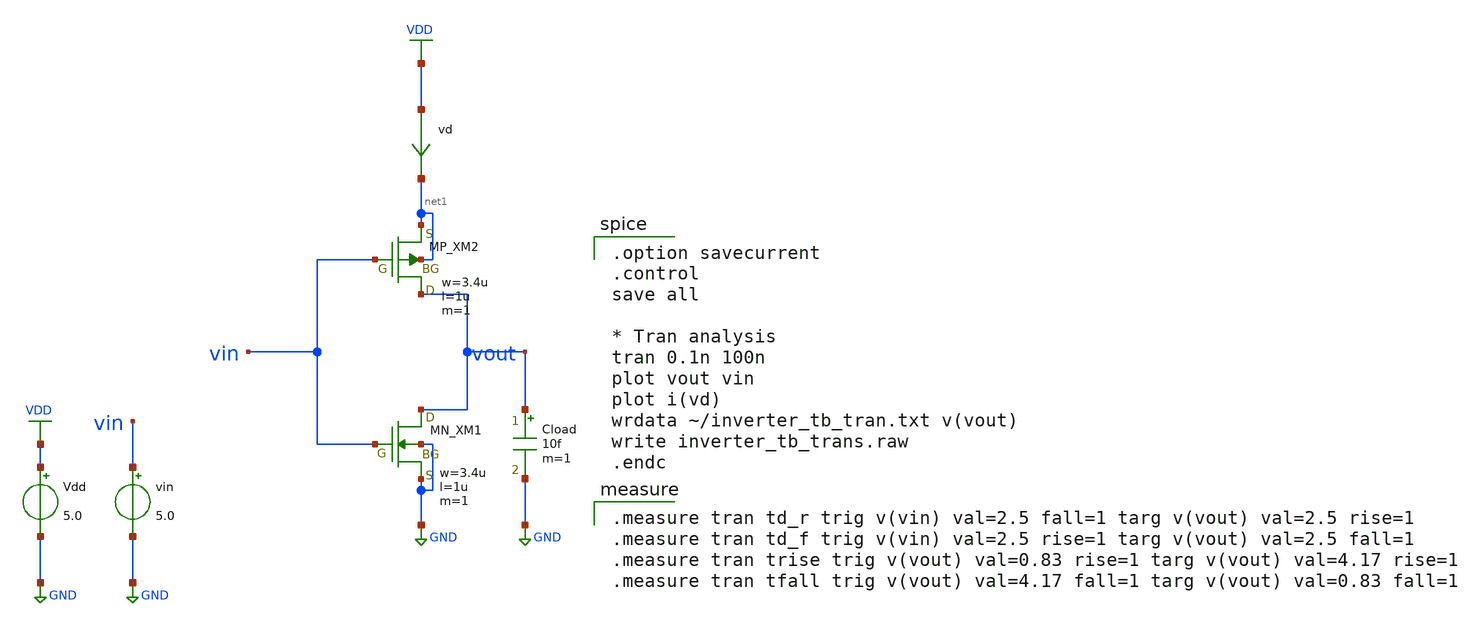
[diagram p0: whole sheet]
** sch_path: member_project/inverter/rikulh/inverter_sim.sch
**.subckt inverter_sim
XM1 vout vin GND GND NMOS w=3.4u l=1u as=0 ad=0 ps=0 pd=0 nrd=0 nrs=0 m=1
XM2 vout vin net1 net1 PMOS w=3.4u l=1u as=0 ad=0 ps=0 pd=0 nrd=0 nrs=0 m=1
vin vin GND 5.0
Vdd VDD GND 5.0
vd VDD net1 0
.save i(vd)
Cload vout GND 10f m=1
**** begin user architecture code
 .include $::LIB/../ip62_models

.option savecurrent
.control
save all

* Tran analysis
tran 0.1n 100n
plot vout vin
plot i(vd)
wrdata ~/inverter_tb_tran.txt v(vout)
write inverter_tb_trans.raw
.endc


.measure tran td_r trig v(vin) val=2.5 fall=1 targ v(vout) val=2.5 rise=1
.measure tran td_f trig v(vin) val=2.5 rise=1 targ v(vout) val=2.5 fall=1
.measure tran trise trig v(vout) val=0.83 rise=1 targ v(vout) val=4.17 rise=1
.measure tran tfall trig v(vout) val=4.17 fall=1 targ v(vout) val=0.83 fall=1

**** end user architecture code
**.ends
.GLOBAL VDD
.GLOBAL GND
.end
